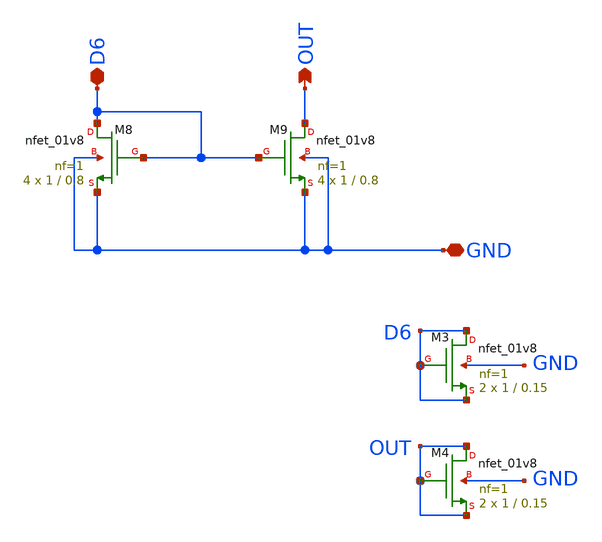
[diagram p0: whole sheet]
** sch_path: nmosdiff/nmosdiff.sch
**.subckt nmosdiff GND OUT D6
*.iopin GND
*.opin OUT
*.iopin D6
XM8 D6 D6 GND GND sky130_fd_pr__nfet_01v8 L=0.8 W=1 nf=1 ad='int((nf+1)/2) * W/nf * 0.29' as='int((nf+2)/2) * W/nf * 0.29'
+ pd='2*int((nf+1)/2) * (W/nf + 0.29)' ps='2*int((nf+2)/2) * (W/nf + 0.29)' nrd='0.29 / W' nrs='0.29 / W'
+ sa=0 sb=0 sd=0 mult=4 m=4
XM9 OUT D6 GND GND sky130_fd_pr__nfet_01v8 L=0.8 W=1 nf=1 ad='int((nf+1)/2) * W/nf * 0.29' as='int((nf+2)/2) * W/nf * 0.29'
+ pd='2*int((nf+1)/2) * (W/nf + 0.29)' ps='2*int((nf+2)/2) * (W/nf + 0.29)' nrd='0.29 / W' nrs='0.29 / W'
+ sa=0 sb=0 sd=0 mult=4 m=4
XM3 D6 D6 D6 GND sky130_fd_pr__nfet_01v8 L=0.15 W=1 nf=1 ad='int((nf+1)/2) * W/nf * 0.29' as='int((nf+2)/2) * W/nf * 0.29'
+ pd='2*int((nf+1)/2) * (W/nf + 0.29)' ps='2*int((nf+2)/2) * (W/nf + 0.29)' nrd='0.29 / W' nrs='0.29 / W'
+ sa=0 sb=0 sd=0 mult=2 m=2
XM4 OUT OUT OUT GND sky130_fd_pr__nfet_01v8 L=0.15 W=1 nf=1 ad='int((nf+1)/2) * W/nf * 0.29' as='int((nf+2)/2) * W/nf * 0.29'
+ pd='2*int((nf+1)/2) * (W/nf + 0.29)' ps='2*int((nf+2)/2) * (W/nf + 0.29)' nrd='0.29 / W' nrs='0.29 / W'
+ sa=0 sb=0 sd=0 mult=2 m=2
**.ends
.end
